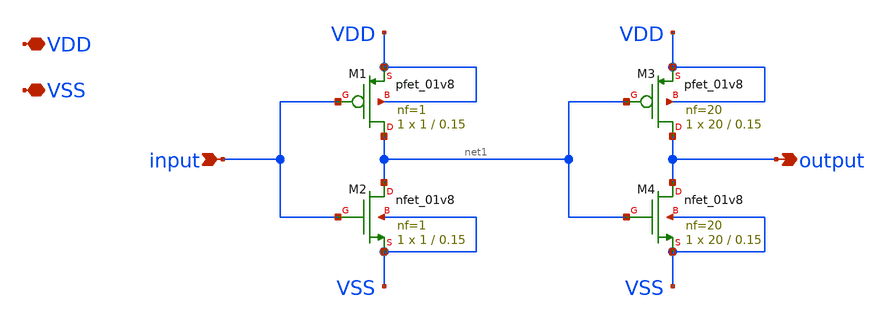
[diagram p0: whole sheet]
** sch_path: xschem/double_inverter.sch
**.subckt double_inverter VDD VSS input output
*.iopin VDD
*.iopin VSS
*.ipin input
*.opin output
XM1 net1 input VDD VDD sky130_fd_pr__pfet_01v8 L=0.15 W=1 nf=1 ad='int((1 + 1)/2) * 1 / 1 * 0.29' as='int((1 + 2)/2) * 1 / 1 * 0.29'
+ pd='2*int((1 + 1)/2) * (1 / 1 + 0.29)' ps='2*int((1 + 2)/2) * (1 / 1 + 0.29)' nrd='0.29 / 1 ' nrs='0.29 / 1 '
+ sa=0 sb=0 sd=0 mult=1 m=1
XM2 net1 input VSS VSS sky130_fd_pr__nfet_01v8 L=0.15 W=1 nf=1 ad='int((1 + 1)/2) * 1 / 1 * 0.29' as='int((1 + 2)/2) * 1 / 1 * 0.29'
+ pd='2*int((1 + 1)/2) * (1 / 1 + 0.29)' ps='2*int((1 + 2)/2) * (1 / 1 + 0.29)' nrd='0.29 / 1 ' nrs='0.29 / 1 '
+ sa=0 sb=0 sd=0 mult=1 m=1
XM3 output net1 VDD VDD sky130_fd_pr__pfet_01v8 L=0.15 W=20 nf=20 ad='int((20 + 1)/2) * 20 / 20 * 0.29'
+ as='int((20 + 2)/2) * 20 / 20 * 0.29' pd='2*int((20 + 1)/2) * (20 / 20 + 0.29)' ps='2*int((20 + 2)/2) * (20 / 20 + 0.29)'
+ nrd='0.29 / 20 ' nrs='0.29 / 20 ' sa=0 sb=0 sd=0 mult=1 m=1
XM4 output net1 VSS VSS sky130_fd_pr__nfet_01v8 L=0.15 W=20 nf=20 ad='int((20 + 1)/2) * 20 / 20 * 0.29'
+ as='int((20 + 2)/2) * 20 / 20 * 0.29' pd='2*int((20 + 1)/2) * (20 / 20 + 0.29)' ps='2*int((20 + 2)/2) * (20 / 20 + 0.29)'
+ nrd='0.29 / 20 ' nrs='0.29 / 20 ' sa=0 sb=0 sd=0 mult=1 m=1
**.ends
.end
